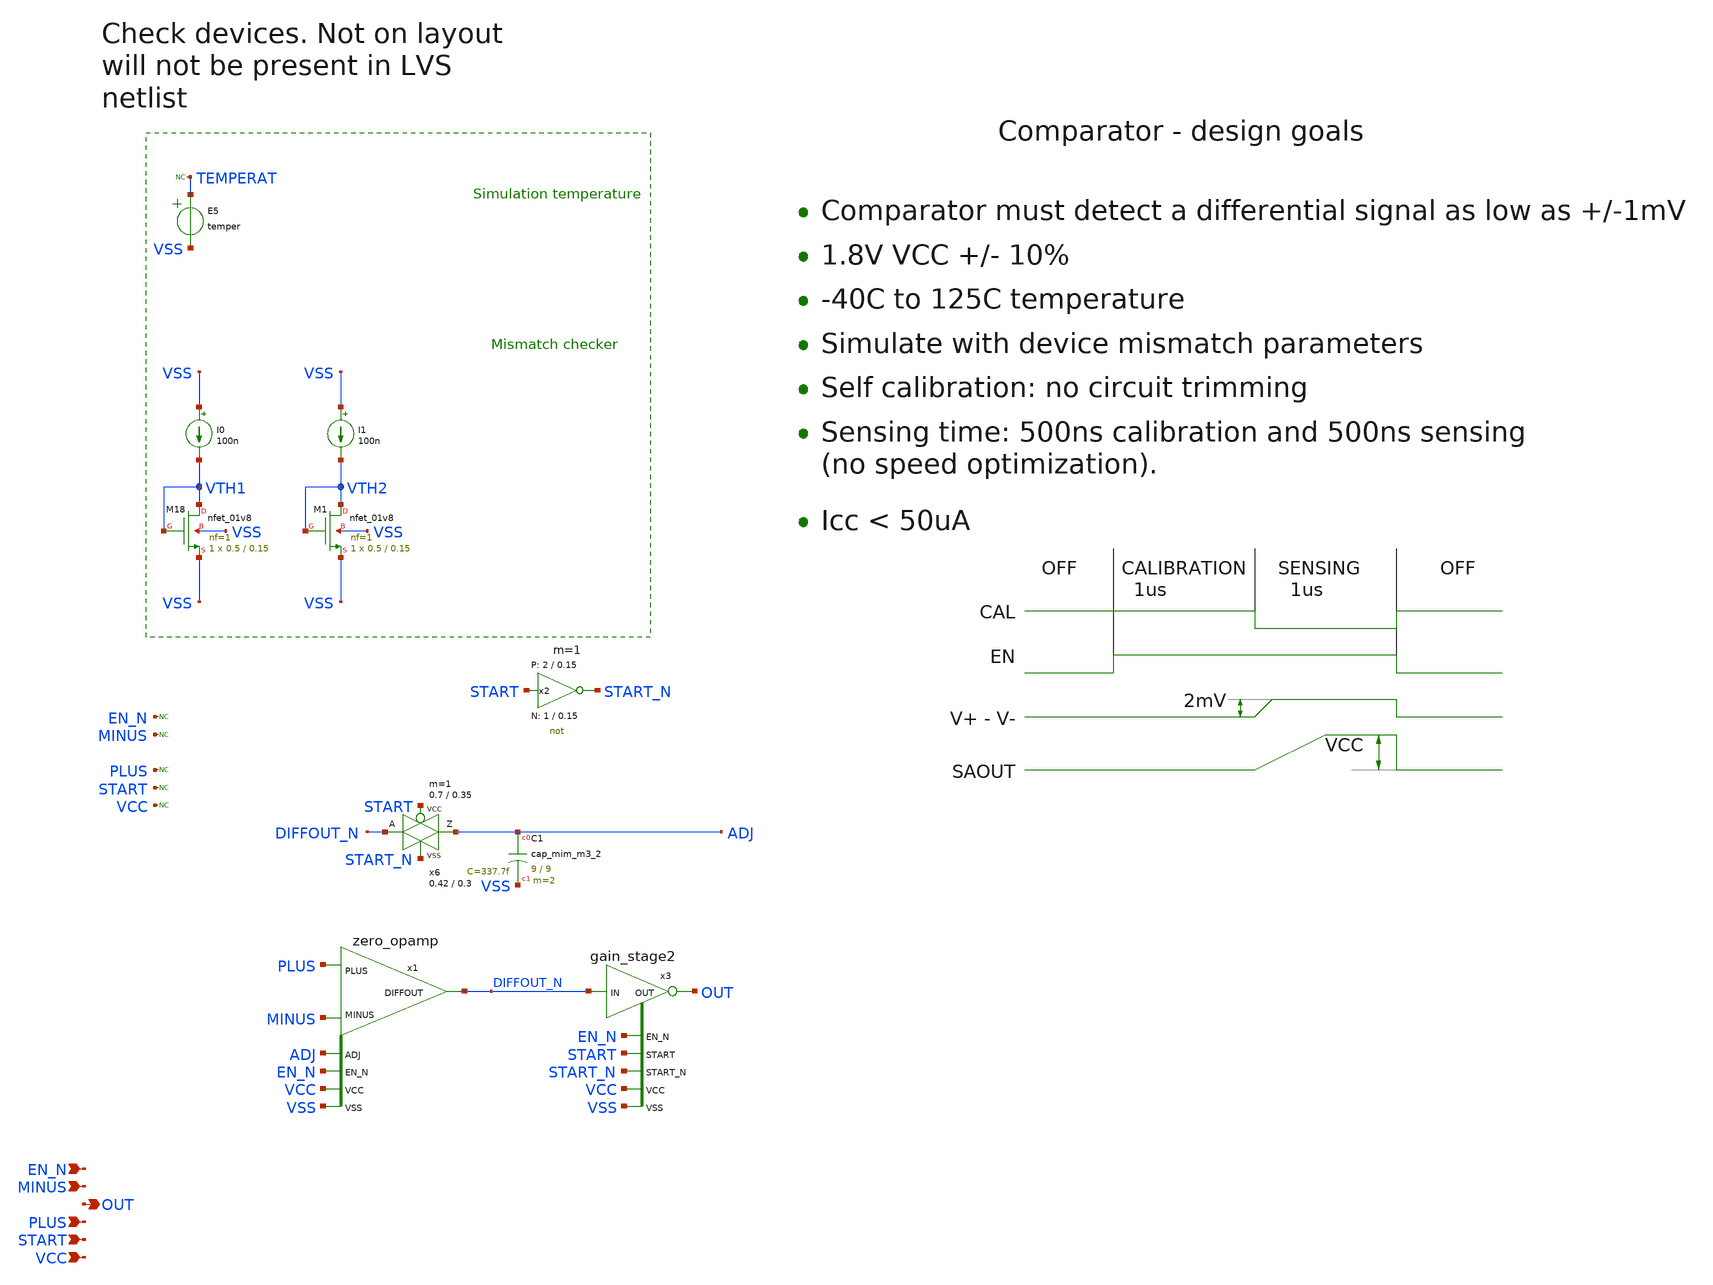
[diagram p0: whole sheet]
** sch_path: sky130A/xschem_libs/sky130_tests_ase/tb_bandgap_opamp/schematic/tb_bandgap_opamp.sch
* Copyright 2021 Stefan Frederik Schippers
* Licensed under the Apache License, Version 2.0 (the "License");
* you may not use this file except in compliance with the License.
* You may obtain a copy of the License at
* https://www.apache.org/licenses/LICENSE-2.0
* Unless required by applicable law or agreed to in writing, software
* distributed under the License is distributed on an "AS IS" BASIS,
* WITHOUT WARRANTIES OR CONDITIONS OF ANY KIND, either express or implied.
* See the License for the specific language governing permissions and
* limitations under the License.
**.subckt tb_bandgap_opamp VCC START PLUS OUT MINUS EN_N
*.ipin VCC
*.ipin START
*.ipin PLUS
*.opin OUT
*.ipin MINUS
*.ipin EN_N
x6 ADJ DIFFOUT_N START START_N VCC VSS passgate_1 W_N=0.42 L_N=0.3 W_P=0.7 L_P=0.35 m=1
XC1 ADJ VSS sky130_fd_pr__cap_mim_m3_2 W=9 L=9 MF=2 m=2
x2 START_N START VCC VSS not W_N=1 L_N=0.15 W_P=2 L_P=0.15 m=1
x1 EN_N MINUS PLUS DIFFOUT_N VCC VSS ADJ zero_opamp
XM18 VTH1 VTH1 VSS VSS sky130_fd_pr__nfet_01v8 L=0.15 W=0.5 nf=1 ad='int((1 + 1)/2) * 0.5 / 1 * 0.29'
+ as='int((1 + 2)/2) * 0.5 / 1 * 0.29' pd='2*int((1 + 1)/2) * (0.5 / 1 + 0.29)' ps='2*int((1 + 2)/2) * (0.5 / 1 + 0.29)'
+ nrd='0.29 / 0.5 ' nrs='0.29 / 0.5 ' sa=0 sb=0 sd=0 mult=1 m=1
I0 VSS VTH1 100n
x3 DIFFOUT_N OUT VCC VSS START_N START EN_N gain_stage2 WN=0.5 WP=1 wcap=9
E5 TEMPERAT VSS VOL=' temper '
* noconn TEMPERAT
* noconn EN_N
* noconn MINUS
* noconn PLUS
* noconn START
* noconn VCC
XM1 VTH2 VTH2 VSS VSS sky130_fd_pr__nfet_01v8 L=0.15 W=0.5 nf=1 ad='int((1 + 1)/2) * 0.5 / 1 * 0.29'
+ as='int((1 + 2)/2) * 0.5 / 1 * 0.29' pd='2*int((1 + 1)/2) * (0.5 / 1 + 0.29)' ps='2*int((1 + 2)/2) * (0.5 / 1 + 0.29)'
+ nrd='0.29 / 0.5 ' nrs='0.29 / 0.5 ' sa=0 sb=0 sd=0 mult=1 m=1
I1 VSS VTH2 100n
**.ends
.end
